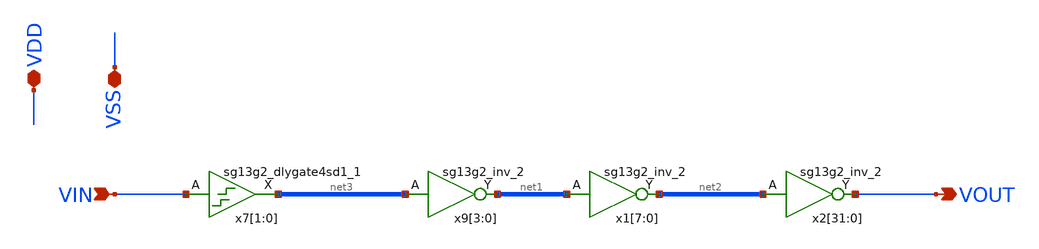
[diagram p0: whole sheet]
** sch_path: Cells/DLine.sch
* IHP-GmbH/IHP-Open-PDK/ihp-sg13g2/libs.tech/xschem/sg13g2_stdcells/sg13g2_inv_2.sch:
* Copyright 2023 IHP PDK Authors
* Licensed under the Apache License, Version 2.0 (the "License");
**.subckt DLine VOUT VIN VDD VSS
*.opin VOUT
*.ipin VIN
*.iopin VDD
*.iopin VSS
x7[1] net3[1] VIN VDD VSS sg13g2_dlygate4sd1_1
x7[0] net3[0] VIN VDD VSS sg13g2_dlygate4sd1_1
x9[3] net1[3] net3[1] VDD VSS sg13g2_inv_2
x9[2] net1[2] net3[0] VDD VSS sg13g2_inv_2
x9[1] net1[1] net3[1] VDD VSS sg13g2_inv_2
x9[0] net1[0] net3[0] VDD VSS sg13g2_inv_2
x1[7] net2[7] net1[3] VDD VSS sg13g2_inv_2
x1[6] net2[6] net1[2] VDD VSS sg13g2_inv_2
x1[5] net2[5] net1[1] VDD VSS sg13g2_inv_2
x1[4] net2[4] net1[0] VDD VSS sg13g2_inv_2
x1[3] net2[3] net1[3] VDD VSS sg13g2_inv_2
x1[2] net2[2] net1[2] VDD VSS sg13g2_inv_2
x1[1] net2[1] net1[1] VDD VSS sg13g2_inv_2
x1[0] net2[0] net1[0] VDD VSS sg13g2_inv_2
x2[31] VOUT net2[7] VDD VSS sg13g2_inv_2
x2[30] VOUT net2[6] VDD VSS sg13g2_inv_2
x2[29] VOUT net2[5] VDD VSS sg13g2_inv_2
x2[28] VOUT net2[4] VDD VSS sg13g2_inv_2
x2[27] VOUT net2[3] VDD VSS sg13g2_inv_2
x2[26] VOUT net2[2] VDD VSS sg13g2_inv_2
x2[25] VOUT net2[1] VDD VSS sg13g2_inv_2
x2[24] VOUT net2[0] VDD VSS sg13g2_inv_2
x2[23] VOUT net2[7] VDD VSS sg13g2_inv_2
x2[22] VOUT net2[6] VDD VSS sg13g2_inv_2
x2[21] VOUT net2[5] VDD VSS sg13g2_inv_2
x2[20] VOUT net2[4] VDD VSS sg13g2_inv_2
x2[19] VOUT net2[3] VDD VSS sg13g2_inv_2
x2[18] VOUT net2[2] VDD VSS sg13g2_inv_2
x2[17] VOUT net2[1] VDD VSS sg13g2_inv_2
x2[16] VOUT net2[0] VDD VSS sg13g2_inv_2
x2[15] VOUT net2[7] VDD VSS sg13g2_inv_2
x2[14] VOUT net2[6] VDD VSS sg13g2_inv_2
x2[13] VOUT net2[5] VDD VSS sg13g2_inv_2
x2[12] VOUT net2[4] VDD VSS sg13g2_inv_2
x2[11] VOUT net2[3] VDD VSS sg13g2_inv_2
x2[10] VOUT net2[2] VDD VSS sg13g2_inv_2
x2[9] VOUT net2[1] VDD VSS sg13g2_inv_2
x2[8] VOUT net2[0] VDD VSS sg13g2_inv_2
x2[7] VOUT net2[7] VDD VSS sg13g2_inv_2
x2[6] VOUT net2[6] VDD VSS sg13g2_inv_2
x2[5] VOUT net2[5] VDD VSS sg13g2_inv_2
x2[4] VOUT net2[4] VDD VSS sg13g2_inv_2
x2[3] VOUT net2[3] VDD VSS sg13g2_inv_2
x2[2] VOUT net2[2] VDD VSS sg13g2_inv_2
x2[1] VOUT net2[1] VDD VSS sg13g2_inv_2
x2[0] VOUT net2[0] VDD VSS sg13g2_inv_2
**.ends

* expanding   symbol:  sg13g2_stdcells/sg13g2_dlygate4sd1_1.sym # of pins=2
** sym_path: sg13g2_stdcells/sg13g2_dlygate4sd1_1.sym
** sch_path: sg13g2_stdcells/sg13g2_dlygate4sd1_1.sch
.subckt sg13g2_dlygate4sd1_1 X A VDD VSS
*.ipin A
*.opin X
*.iopin VDD
*.iopin VSS
XM1 net2 A VSS VSS sg13_lv_nmos w=420.00n l=130.00n ng=1 m=1 mm_ok=1
XM2 net1 net2 VSS VSS sg13_lv_nmos w=420.00n l=130.00n ng=1 m=1 mm_ok=1
XM3 net3 net1 VSS VSS sg13_lv_nmos w=420.00n l=130.00n ng=1 m=1 mm_ok=1
XM4 X net3 VSS VSS sg13_lv_nmos w=740.00n l=130.00n ng=1 m=1 mm_ok=1
XM5 net2 A VDD VDD sg13_lv_pmos w=420.00n l=130.00n ng=1 m=1 mm_ok=1
XM6 net1 net2 VDD VDD sg13_lv_pmos w=1.000u l=130.00n ng=1 m=1 mm_ok=1
XM7 net3 net1 VDD VDD sg13_lv_pmos w=1.000u l=130.00n ng=1 m=1 mm_ok=1
XM8 X net3 VDD VDD sg13_lv_pmos w=1.12u l=130.00n ng=1 m=1 mm_ok=1
.ends


* expanding   symbol:  sg13g2_stdcells/sg13g2_inv_2.sym # of pins=2
** sym_path: sg13g2_stdcells/sg13g2_inv_2.sym
** sch_path: sg13g2_stdcells/sg13g2_inv_2.sch
.subckt sg13g2_inv_2 Y A VDD VSS
*.opin Y
*.ipin A
*.iopin VDD
*.iopin VSS
XM1 Y A VSS VSS sg13_lv_nmos w=1.48u l=130.00n ng=2 m=1 mm_ok=1
XM2 Y A VDD VDD sg13_lv_pmos w=2.24u l=130.00n ng=2 m=1 mm_ok=1
.ends

.end
